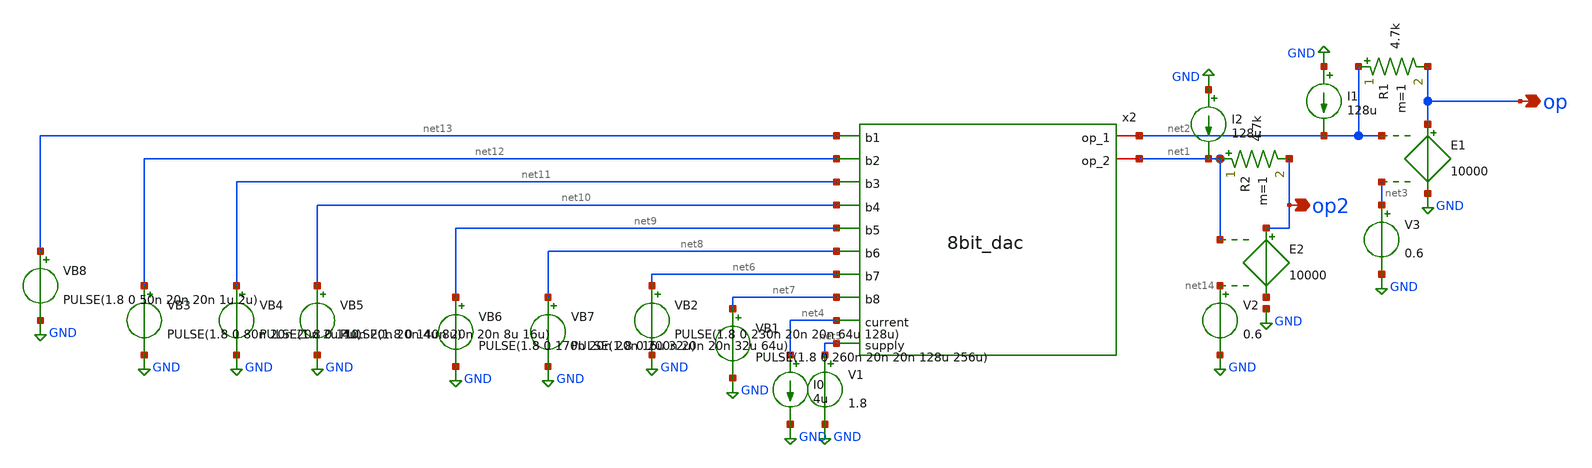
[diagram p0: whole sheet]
** sch_path: ANALOG_PERIPHERAL/DAC/schematic/8bit_dac_tb.sch
**.subckt 8bit_dac_tb op op2
*.opin op
*.opin op2
V2 net14 GND 0.6
V3 net3 GND 0.6
I0 net4 GND 4u
V1 net5 GND 1.8
VB2 net6 GND PULSE(1.8 0 230n 20n 20n 64u 128u)
VB1 net7 GND PULSE(1.8 0 260n 20n 20n 128u 256u)
VB8 net13 GND PULSE(1.8 0 50n 20n 20n 1u 2u)
VB3 net12 GND PULSE(1.8 0 80n 20n 20n 2u 4u)
VB4 net11 GND PULSE(1.8 0 110n 20n 20n 4u 8u)
VB5 net10 GND PULSE(1.8 0 140n 20n 20n 8u 16u)
VB6 net9 GND PULSE(1.8 0 170n 20n 20n 16u 32u)
VB7 net8 GND PULSE(1.8 0 200n 20n 20n 32u 64u)
E1 op GND net2 net3 10000
R1 net2 op 4.7k m=1
E2 op2 net15 net1 net14 10000
R2 net1 op2 4.7k m=1
I1 GND net2 128u
I2 GND net1 128u
x2 net13 net12 net11 net10 net9 net8 net6 net7 net2 net1 net4 net5 8bit_dac
**** begin user architecture code




* transient analysis
.tran 1n 270u
*.op
.control
run


plot -i(V4)

plot v(op)
plot v(op2)


write dac_32tb.raw
.endc

.end


* ngspice commands




** opencircuitdesign pdks install
.lib $::SKYWATER_MODELS/sky130.lib.spice tt

**** end user architecture code
**.ends
.GLOBAL GND
.end
